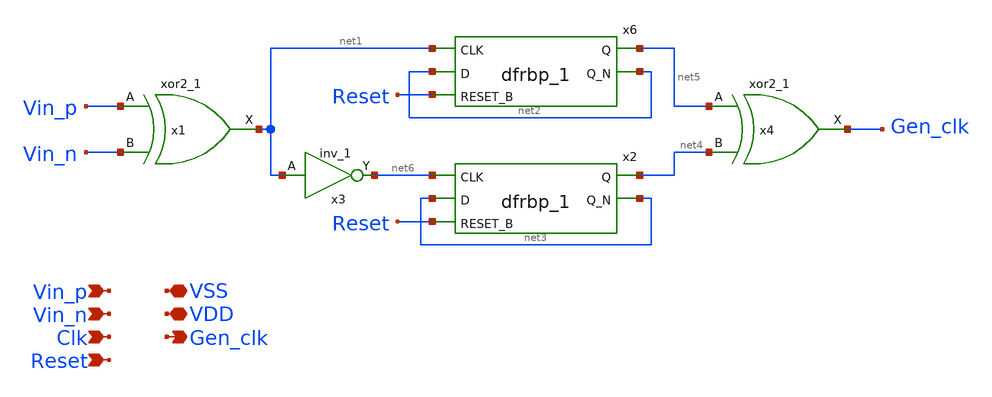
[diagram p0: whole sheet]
** sch_path: xschem/src/xor_clock_gen/xor_clock_gen.sch
**.subckt xor_clock_gen Vin_p VSS Gen_clk VDD Vin_n Clk Reset
*.ipin Vin_p
*.iopin VSS
*.opin Gen_clk
*.iopin VDD
*.ipin Vin_n
*.ipin Clk
*.ipin Reset
x1 Vin_p Vin_n VSS VSS VDD VDD net1 sky130_fd_sc_hd__xor2_1
x3 net1 VSS VSS VDD VDD net6 sky130_fd_sc_hd__inv_1
x6 net1 net2 Reset VSS VSS VDD VDD net5 net2 sky130_fd_sc_hd__dfrbp_1
x2 net6 net3 Reset VSS VSS VDD VDD net4 net3 sky130_fd_sc_hd__dfrbp_1
x4 net5 net4 VSS VSS VDD VDD Gen_clk sky130_fd_sc_hd__xor2_1
**.ends
.end
